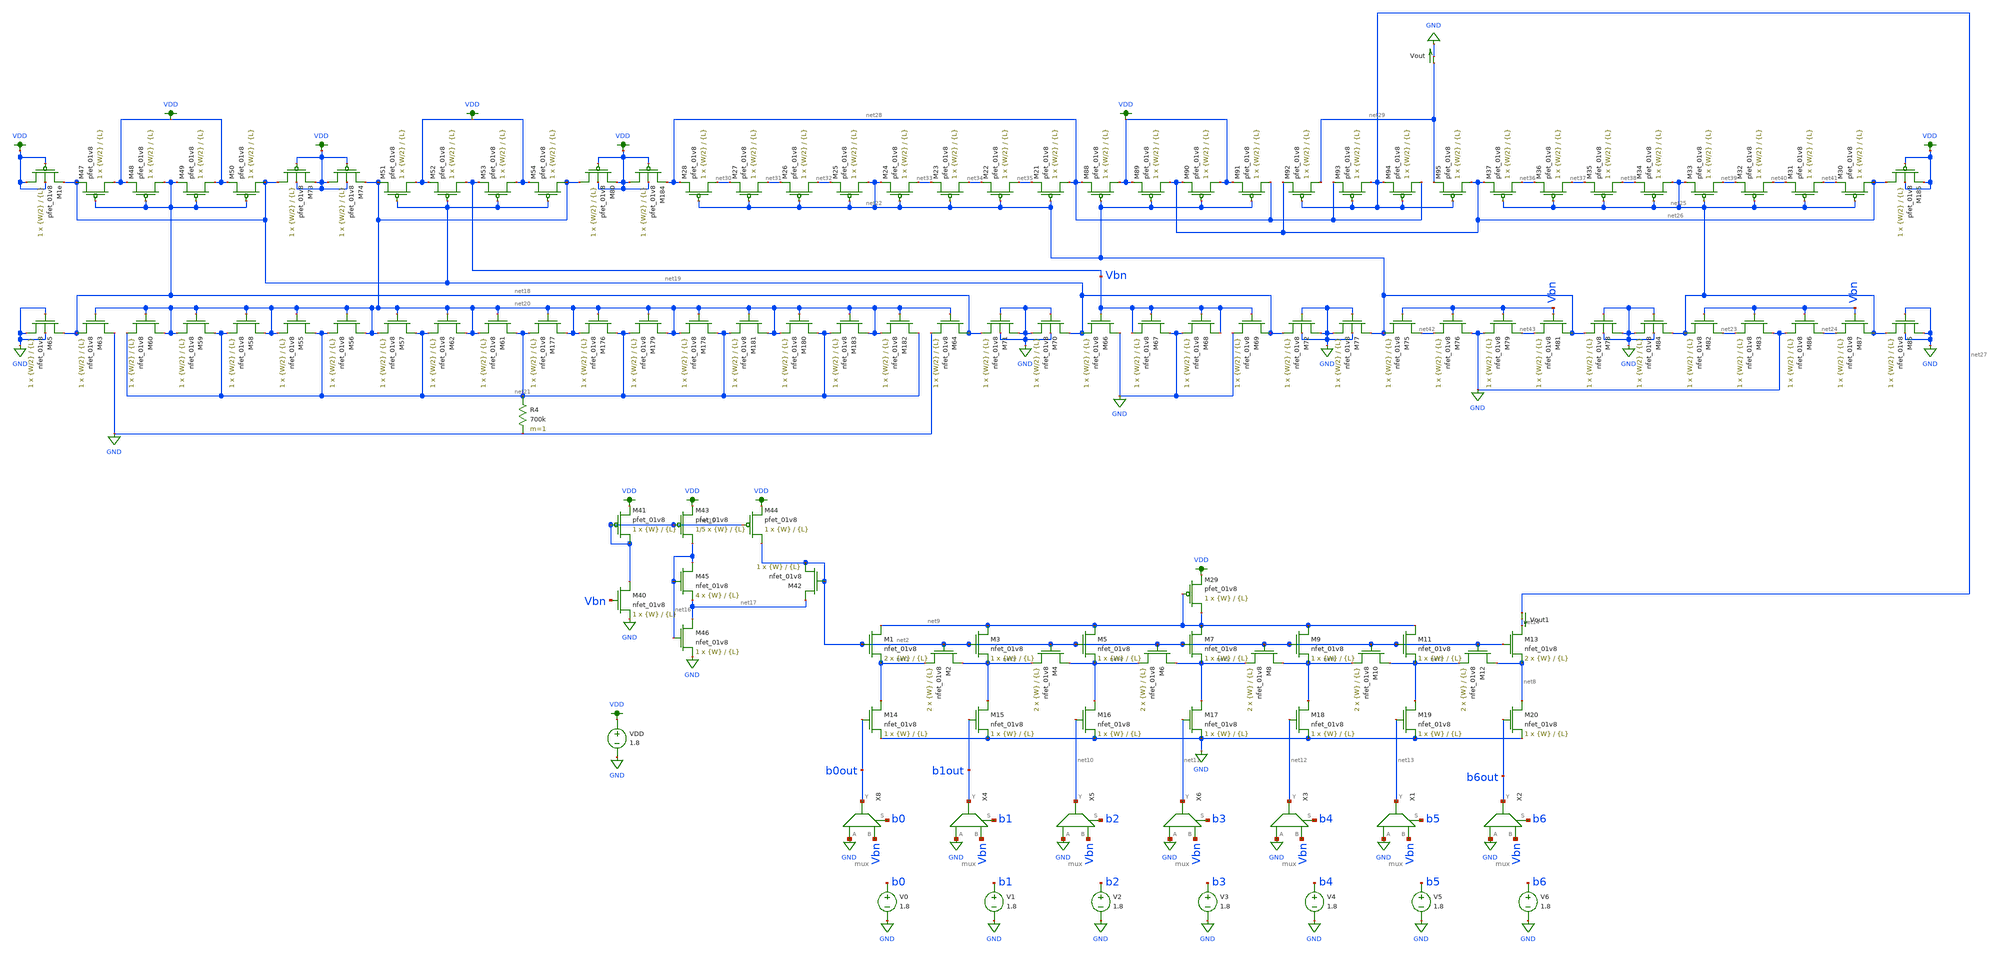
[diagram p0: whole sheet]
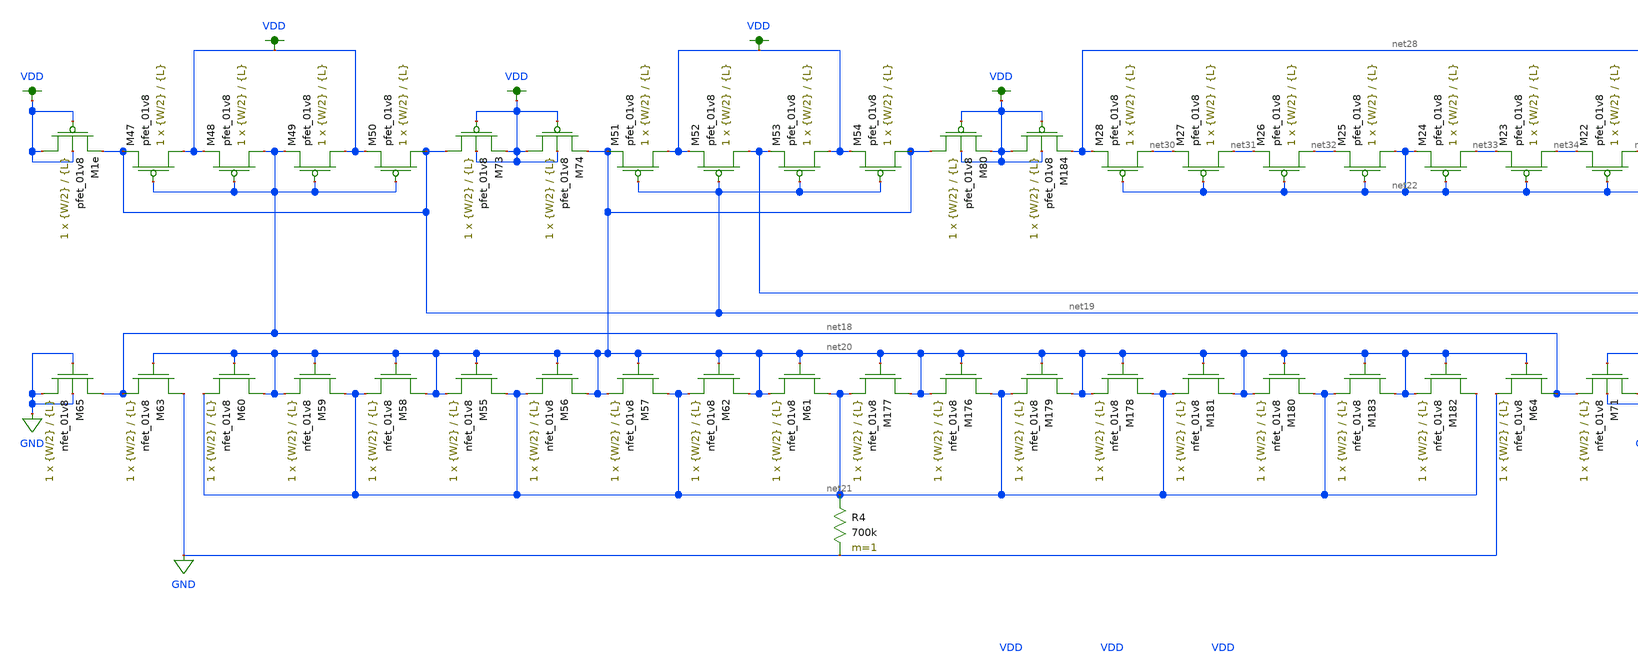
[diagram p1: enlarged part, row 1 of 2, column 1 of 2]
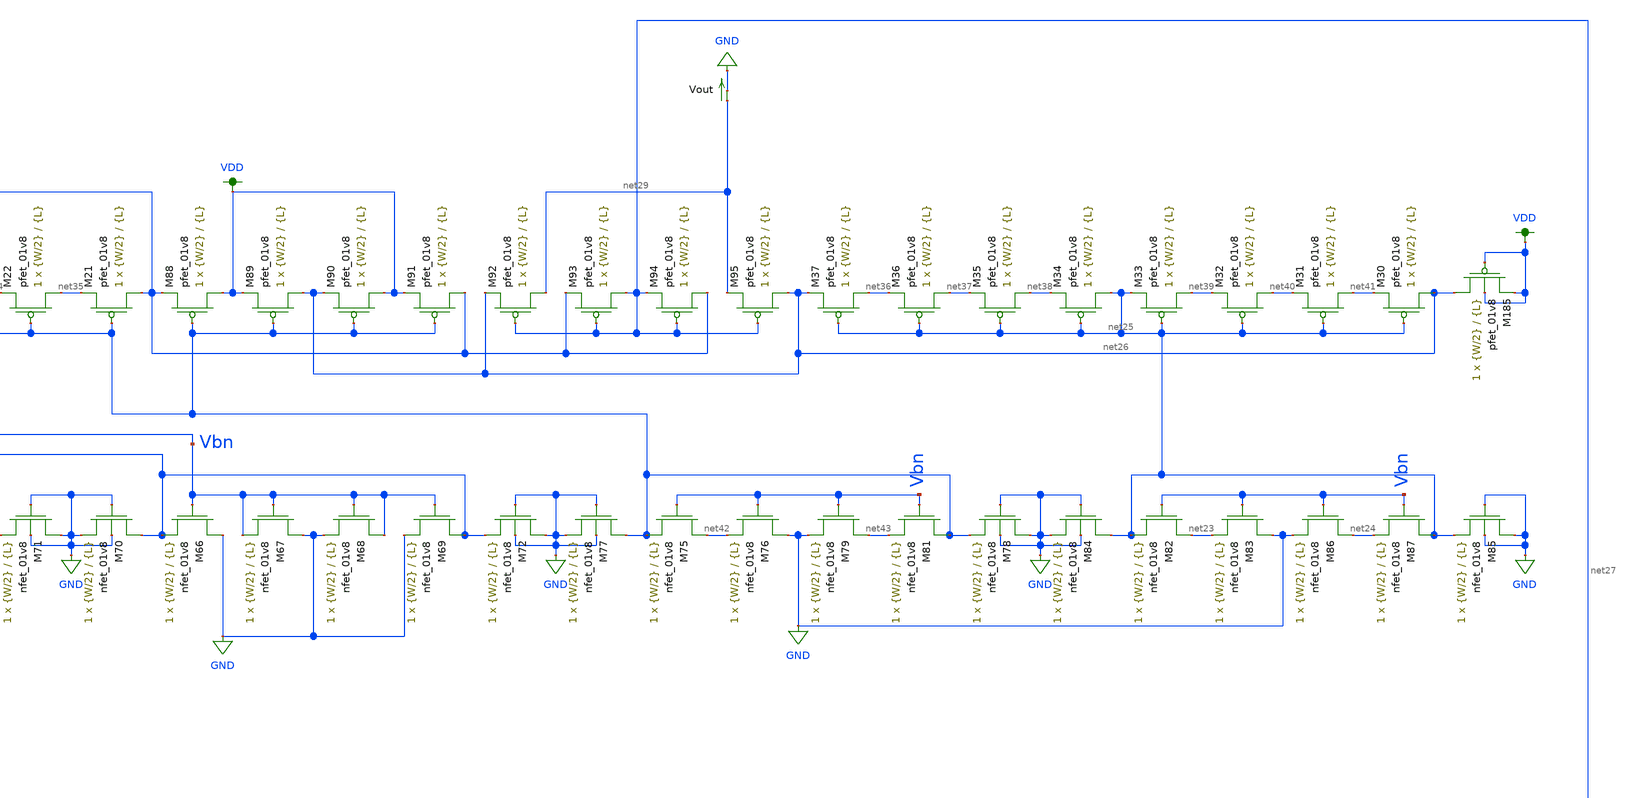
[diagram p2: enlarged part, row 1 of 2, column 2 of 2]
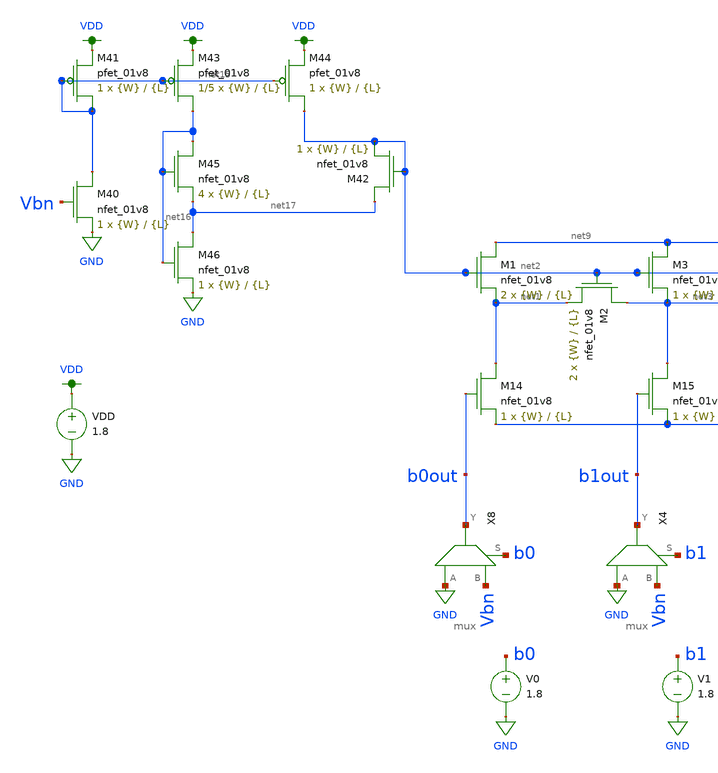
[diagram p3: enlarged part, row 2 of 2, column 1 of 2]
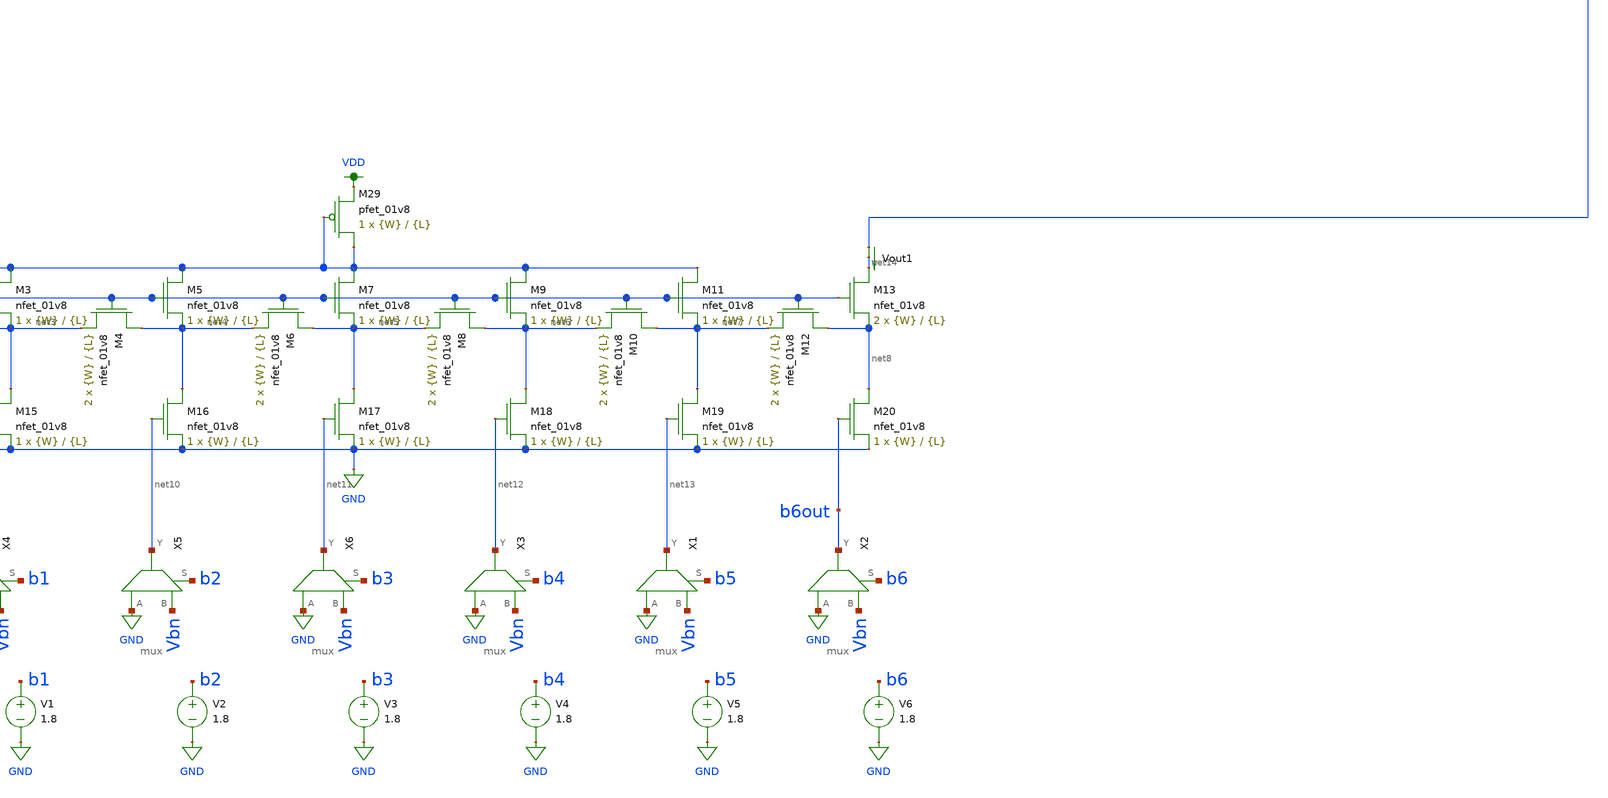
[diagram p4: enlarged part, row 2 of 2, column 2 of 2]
** sch_path: schematics/dac_dnl_inl_current_mirror_lds.sch
**.subckt dac_dnl_inl_current_mirror_lds
XM1 net9 net2 net1 GND sky130_fd_pr__nfet_01v8 L={L} W={W} nf=1 ad='int((nf+1)/2) * W/nf * 0.29' as='int((nf+2)/2) * W/nf * 0.29'
+ pd='2*int((nf+1)/2) * (W/nf + 0.29)' ps='2*int((nf+2)/2) * (W/nf + 0.29)' nrd='0.29 / W' nrs='0.29 / W'
+ sa=0 sb=0 sd=0 mult=2 m=2
XM2 net3 net2 net1 GND sky130_fd_pr__nfet_01v8 L={L} W={W} nf=1 ad='int((nf+1)/2) * W/nf * 0.29' as='int((nf+2)/2) * W/nf * 0.29'
+ pd='2*int((nf+1)/2) * (W/nf + 0.29)' ps='2*int((nf+2)/2) * (W/nf + 0.29)' nrd='0.29 / W' nrs='0.29 / W'
+ sa=0 sb=0 sd=0 mult=2 m=2
XM3 net9 net2 net3 GND sky130_fd_pr__nfet_01v8 L={L} W={W} nf=1 ad='int((nf+1)/2) * W/nf * 0.29' as='int((nf+2)/2) * W/nf * 0.29'
+ pd='2*int((nf+1)/2) * (W/nf + 0.29)' ps='2*int((nf+2)/2) * (W/nf + 0.29)' nrd='0.29 / W' nrs='0.29 / W'
+ sa=0 sb=0 sd=0 mult=1 m=1
XM4 net4 net2 net3 GND sky130_fd_pr__nfet_01v8 L={L} W={W} nf=1 ad='int((nf+1)/2) * W/nf * 0.29' as='int((nf+2)/2) * W/nf * 0.29'
+ pd='2*int((nf+1)/2) * (W/nf + 0.29)' ps='2*int((nf+2)/2) * (W/nf + 0.29)' nrd='0.29 / W' nrs='0.29 / W'
+ sa=0 sb=0 sd=0 mult=2 m=2
XM5 net9 net2 net4 GND sky130_fd_pr__nfet_01v8 L={L} W={W} nf=1 ad='int((nf+1)/2) * W/nf * 0.29' as='int((nf+2)/2) * W/nf * 0.29'
+ pd='2*int((nf+1)/2) * (W/nf + 0.29)' ps='2*int((nf+2)/2) * (W/nf + 0.29)' nrd='0.29 / W' nrs='0.29 / W'
+ sa=0 sb=0 sd=0 mult=1 m=1
XM6 net5 net2 net4 GND sky130_fd_pr__nfet_01v8 L={L} W={W} nf=1 ad='int((nf+1)/2) * W/nf * 0.29' as='int((nf+2)/2) * W/nf * 0.29'
+ pd='2*int((nf+1)/2) * (W/nf + 0.29)' ps='2*int((nf+2)/2) * (W/nf + 0.29)' nrd='0.29 / W' nrs='0.29 / W'
+ sa=0 sb=0 sd=0 mult=2 m=2
XM7 net9 net2 net5 GND sky130_fd_pr__nfet_01v8 L={L} W={W} nf=1 ad='int((nf+1)/2) * W/nf * 0.29' as='int((nf+2)/2) * W/nf * 0.29'
+ pd='2*int((nf+1)/2) * (W/nf + 0.29)' ps='2*int((nf+2)/2) * (W/nf + 0.29)' nrd='0.29 / W' nrs='0.29 / W'
+ sa=0 sb=0 sd=0 mult=1 m=1
XM8 net6 net2 net5 GND sky130_fd_pr__nfet_01v8 L={L} W={W} nf=1 ad='int((nf+1)/2) * W/nf * 0.29' as='int((nf+2)/2) * W/nf * 0.29'
+ pd='2*int((nf+1)/2) * (W/nf + 0.29)' ps='2*int((nf+2)/2) * (W/nf + 0.29)' nrd='0.29 / W' nrs='0.29 / W'
+ sa=0 sb=0 sd=0 mult=2 m=2
XM9 net9 net2 net6 GND sky130_fd_pr__nfet_01v8 L={L} W={W} nf=1 ad='int((nf+1)/2) * W/nf * 0.29' as='int((nf+2)/2) * W/nf * 0.29'
+ pd='2*int((nf+1)/2) * (W/nf + 0.29)' ps='2*int((nf+2)/2) * (W/nf + 0.29)' nrd='0.29 / W' nrs='0.29 / W'
+ sa=0 sb=0 sd=0 mult=1 m=1
XM10 net7 net2 net6 GND sky130_fd_pr__nfet_01v8 L={L} W={W} nf=1 ad='int((nf+1)/2) * W/nf * 0.29' as='int((nf+2)/2) * W/nf * 0.29'
+ pd='2*int((nf+1)/2) * (W/nf + 0.29)' ps='2*int((nf+2)/2) * (W/nf + 0.29)' nrd='0.29 / W' nrs='0.29 / W'
+ sa=0 sb=0 sd=0 mult=2 m=2
XM11 net9 net2 net7 GND sky130_fd_pr__nfet_01v8 L={L} W={W} nf=1 ad='int((nf+1)/2) * W/nf * 0.29' as='int((nf+2)/2) * W/nf * 0.29'
+ pd='2*int((nf+1)/2) * (W/nf + 0.29)' ps='2*int((nf+2)/2) * (W/nf + 0.29)' nrd='0.29 / W' nrs='0.29 / W'
+ sa=0 sb=0 sd=0 mult=1 m=1
XM12 net8 net2 net7 GND sky130_fd_pr__nfet_01v8 L={L} W={W} nf=1 ad='int((nf+1)/2) * W/nf * 0.29' as='int((nf+2)/2) * W/nf * 0.29'
+ pd='2*int((nf+1)/2) * (W/nf + 0.29)' ps='2*int((nf+2)/2) * (W/nf + 0.29)' nrd='0.29 / W' nrs='0.29 / W'
+ sa=0 sb=0 sd=0 mult=2 m=2
XM13 net14 net2 net8 GND sky130_fd_pr__nfet_01v8 L={L} W={W} nf=1 ad='int((nf+1)/2) * W/nf * 0.29' as='int((nf+2)/2) * W/nf * 0.29'
+ pd='2*int((nf+1)/2) * (W/nf + 0.29)' ps='2*int((nf+2)/2) * (W/nf + 0.29)' nrd='0.29 / W' nrs='0.29 / W'
+ sa=0 sb=0 sd=0 mult=2 m=2
XM14 net1 b0out GND GND sky130_fd_pr__nfet_01v8 L={L} W={W} nf=1 ad='int((nf+1)/2) * W/nf * 0.29' as='int((nf+2)/2) * W/nf * 0.29'
+ pd='2*int((nf+1)/2) * (W/nf + 0.29)' ps='2*int((nf+2)/2) * (W/nf + 0.29)' nrd='0.29 / W' nrs='0.29 / W'
+ sa=0 sb=0 sd=0 mult=1 m=1
XM15 net3 b1out GND GND sky130_fd_pr__nfet_01v8 L={L} W={W} nf=1 ad='int((nf+1)/2) * W/nf * 0.29' as='int((nf+2)/2) * W/nf * 0.29'
+ pd='2*int((nf+1)/2) * (W/nf + 0.29)' ps='2*int((nf+2)/2) * (W/nf + 0.29)' nrd='0.29 / W' nrs='0.29 / W'
+ sa=0 sb=0 sd=0 mult=1 m=1
XM16 net4 net10 GND GND sky130_fd_pr__nfet_01v8 L={L} W={W} nf=1 ad='int((nf+1)/2) * W/nf * 0.29' as='int((nf+2)/2) * W/nf * 0.29'
+ pd='2*int((nf+1)/2) * (W/nf + 0.29)' ps='2*int((nf+2)/2) * (W/nf + 0.29)' nrd='0.29 / W' nrs='0.29 / W'
+ sa=0 sb=0 sd=0 mult=1 m=1
XM17 net5 net11 GND GND sky130_fd_pr__nfet_01v8 L={L} W={W} nf=1 ad='int((nf+1)/2) * W/nf * 0.29' as='int((nf+2)/2) * W/nf * 0.29'
+ pd='2*int((nf+1)/2) * (W/nf + 0.29)' ps='2*int((nf+2)/2) * (W/nf + 0.29)' nrd='0.29 / W' nrs='0.29 / W'
+ sa=0 sb=0 sd=0 mult=1 m=1
XM18 net6 net12 GND GND sky130_fd_pr__nfet_01v8 L={L} W={W} nf=1 ad='int((nf+1)/2) * W/nf * 0.29' as='int((nf+2)/2) * W/nf * 0.29'
+ pd='2*int((nf+1)/2) * (W/nf + 0.29)' ps='2*int((nf+2)/2) * (W/nf + 0.29)' nrd='0.29 / W' nrs='0.29 / W'
+ sa=0 sb=0 sd=0 mult=1 m=1
XM19 net7 net13 GND GND sky130_fd_pr__nfet_01v8 L={L} W={W} nf=1 ad='int((nf+1)/2) * W/nf * 0.29' as='int((nf+2)/2) * W/nf * 0.29'
+ pd='2*int((nf+1)/2) * (W/nf + 0.29)' ps='2*int((nf+2)/2) * (W/nf + 0.29)' nrd='0.29 / W' nrs='0.29 / W'
+ sa=0 sb=0 sd=0 mult=1 m=1
XM20 net8 b6out GND GND sky130_fd_pr__nfet_01v8 L={L} W={W} nf=1 ad='int((nf+1)/2) * W/nf * 0.29' as='int((nf+2)/2) * W/nf * 0.29'
+ pd='2*int((nf+1)/2) * (W/nf + 0.29)' ps='2*int((nf+2)/2) * (W/nf + 0.29)' nrd='0.29 / W' nrs='0.29 / W'
+ sa=0 sb=0 sd=0 mult=1 m=1
V0 b0 GND 1.8
V1 b1 GND 1.8
V2 b2 GND 1.8
V3 b3 GND 1.8
V4 b4 GND 1.8
V5 b5 GND 1.8
V6 b6 GND 1.8
VDD VDD GND 1.8
XM29 net9 net9 VDD VDD sky130_fd_pr__pfet_01v8 L={L} W={W} nf=1 ad='int((nf+1)/2) * W/nf * 0.29' as='int((nf+2)/2) * W/nf * 0.29'
+ pd='2*int((nf+1)/2) * (W/nf + 0.29)' ps='2*int((nf+2)/2) * (W/nf + 0.29)' nrd='0.29 / W' nrs='0.29 / W'
+ sa=0 sb=0 sd=0 mult=1 m=1
X8 GND Vbn b0out b0 mux
X4 GND Vbn b1out b1 mux
X5 GND Vbn net10 b2 mux
X6 GND Vbn net11 b3 mux
X3 GND Vbn net12 b4 mux
X1 GND Vbn net13 b5 mux
X2 GND Vbn b6out b6 mux
Vout1 net27 net14 0
.save i(vout1)
XM40 net15 Vbn GND GND sky130_fd_pr__nfet_01v8 L={L} W={W} nf=1 ad='int((nf+1)/2) * W/nf * 0.29' as='int((nf+2)/2) * W/nf * 0.29'
+ pd='2*int((nf+1)/2) * (W/nf + 0.29)' ps='2*int((nf+2)/2) * (W/nf + 0.29)' nrd='0.29 / W' nrs='0.29 / W'
+ sa=0 sb=0 sd=0 mult=1 m=1
XM41 net15 net15 VDD VDD sky130_fd_pr__pfet_01v8 L={L} W={W} nf=1 ad='int((nf+1)/2) * W/nf * 0.29' as='int((nf+2)/2) * W/nf * 0.29'
+ pd='2*int((nf+1)/2) * (W/nf + 0.29)' ps='2*int((nf+2)/2) * (W/nf + 0.29)' nrd='0.29 / W' nrs='0.29 / W'
+ sa=0 sb=0 sd=0 mult=1 m=1
XM42 net17 net2 net2 GND sky130_fd_pr__nfet_01v8 L={L} W={W} nf=1 ad='int((nf+1)/2) * W/nf * 0.29' as='int((nf+2)/2) * W/nf * 0.29'
+ pd='2*int((nf+1)/2) * (W/nf + 0.29)' ps='2*int((nf+2)/2) * (W/nf + 0.29)' nrd='0.29 / W' nrs='0.29 / W'
+ sa=0 sb=0 sd=0 mult=1 m=1
XM43 net16 net15 VDD VDD sky130_fd_pr__pfet_01v8 L={L} W={W} nf=1 ad='int((nf+1)/2) * W/nf * 0.29' as='int((nf+2)/2) * W/nf * 0.29'
+ pd='2*int((nf+1)/2) * (W/nf + 0.29)' ps='2*int((nf+2)/2) * (W/nf + 0.29)' nrd='0.29 / W' nrs='0.29 / W'
+ sa=0 sb=0 sd=0 mult=1/5 m=1/5
XM44 net2 net15 VDD VDD sky130_fd_pr__pfet_01v8 L={L} W={W} nf=1 ad='int((nf+1)/2) * W/nf * 0.29' as='int((nf+2)/2) * W/nf * 0.29'
+ pd='2*int((nf+1)/2) * (W/nf + 0.29)' ps='2*int((nf+2)/2) * (W/nf + 0.29)' nrd='0.29 / W' nrs='0.29 / W'
+ sa=0 sb=0 sd=0 mult=1 m=1
XM45 net16 net16 net17 GND sky130_fd_pr__nfet_01v8 L={L} W={W} nf=1 ad='int((nf+1)/2) * W/nf * 0.29'
+ as='int((nf+2)/2) * W/nf * 0.29' pd='2*int((nf+1)/2) * (W/nf + 0.29)' ps='2*int((nf+2)/2) * (W/nf + 0.29)'
+ nrd='0.29 / W' nrs='0.29 / W' sa=0 sb=0 sd=0 mult=4 m=4
XM46 net17 net16 GND GND sky130_fd_pr__nfet_01v8 L={L} W={W} nf=1 ad='int((nf+1)/2) * W/nf * 0.29' as='int((nf+2)/2) * W/nf * 0.29'
+ pd='2*int((nf+1)/2) * (W/nf + 0.29)' ps='2*int((nf+2)/2) * (W/nf + 0.29)' nrd='0.29 / W' nrs='0.29 / W'
+ sa=0 sb=0 sd=0 mult=1 m=1
XM47 VDD net18 net19 VDD sky130_fd_pr__pfet_01v8 L={L} W={W/2} nf=1 ad='int((nf+1)/2) * W/nf * 0.29'
+ as='int((nf+2)/2) * W/nf * 0.29' pd='2*int((nf+1)/2) * (W/nf + 0.29)' ps='2*int((nf+2)/2) * (W/nf + 0.29)'
+ nrd='0.29 / W' nrs='0.29 / W' sa=0 sb=0 sd=0 mult=1 m=1
XM48 net18 net18 VDD VDD sky130_fd_pr__pfet_01v8 L={L} W={W/2} nf=1 ad='int((nf+1)/2) * W/nf * 0.29'
+ as='int((nf+2)/2) * W/nf * 0.29' pd='2*int((nf+1)/2) * (W/nf + 0.29)' ps='2*int((nf+2)/2) * (W/nf + 0.29)'
+ nrd='0.29 / W' nrs='0.29 / W' sa=0 sb=0 sd=0 mult=1 m=1
XM49 VDD net18 net18 VDD sky130_fd_pr__pfet_01v8 L={L} W={W/2} nf=1 ad='int((nf+1)/2) * W/nf * 0.29'
+ as='int((nf+2)/2) * W/nf * 0.29' pd='2*int((nf+1)/2) * (W/nf + 0.29)' ps='2*int((nf+2)/2) * (W/nf + 0.29)'
+ nrd='0.29 / W' nrs='0.29 / W' sa=0 sb=0 sd=0 mult=1 m=1
XM50 net19 net18 VDD VDD sky130_fd_pr__pfet_01v8 L={L} W={W/2} nf=1 ad='int((nf+1)/2) * W/nf * 0.29'
+ as='int((nf+2)/2) * W/nf * 0.29' pd='2*int((nf+1)/2) * (W/nf + 0.29)' ps='2*int((nf+2)/2) * (W/nf + 0.29)'
+ nrd='0.29 / W' nrs='0.29 / W' sa=0 sb=0 sd=0 mult=1 m=1
XM51 VDD net19 net20 VDD sky130_fd_pr__pfet_01v8 L={L} W={W/2} nf=1 ad='int((nf+1)/2) * W/nf * 0.29'
+ as='int((nf+2)/2) * W/nf * 0.29' pd='2*int((nf+1)/2) * (W/nf + 0.29)' ps='2*int((nf+2)/2) * (W/nf + 0.29)'
+ nrd='0.29 / W' nrs='0.29 / W' sa=0 sb=0 sd=0 mult=1 m=1
XM52 Vbn net19 VDD VDD sky130_fd_pr__pfet_01v8 L={L} W={W/2} nf=1 ad='int((nf+1)/2) * W/nf * 0.29' as='int((nf+2)/2) * W/nf * 0.29'
+ pd='2*int((nf+1)/2) * (W/nf + 0.29)' ps='2*int((nf+2)/2) * (W/nf + 0.29)' nrd='0.29 / W' nrs='0.29 / W'
+ sa=0 sb=0 sd=0 mult=1 m=1
XM53 VDD net19 Vbn VDD sky130_fd_pr__pfet_01v8 L={L} W={W/2} nf=1 ad='int((nf+1)/2) * W/nf * 0.29' as='int((nf+2)/2) * W/nf * 0.29'
+ pd='2*int((nf+1)/2) * (W/nf + 0.29)' ps='2*int((nf+2)/2) * (W/nf + 0.29)' nrd='0.29 / W' nrs='0.29 / W'
+ sa=0 sb=0 sd=0 mult=1 m=1
XM54 net20 net19 VDD VDD sky130_fd_pr__pfet_01v8 L={L} W={W/2} nf=1 ad='int((nf+1)/2) * W/nf * 0.29'
+ as='int((nf+2)/2) * W/nf * 0.29' pd='2*int((nf+1)/2) * (W/nf + 0.29)' ps='2*int((nf+2)/2) * (W/nf + 0.29)'
+ nrd='0.29 / W' nrs='0.29 / W' sa=0 sb=0 sd=0 mult=1 m=1
XM55 net21 net20 net20 GND sky130_fd_pr__nfet_01v8 L={L} W={W/2} nf=1 ad='int((nf+1)/2) * W/nf * 0.29'
+ as='int((nf+2)/2) * W/nf * 0.29' pd='2*int((nf+1)/2) * (W/nf + 0.29)' ps='2*int((nf+2)/2) * (W/nf + 0.29)'
+ nrd='0.29 / W' nrs='0.29 / W' sa=0 sb=0 sd=0 mult=1 m=1
XM56 net20 net20 net21 GND sky130_fd_pr__nfet_01v8 L={L} W={W/2} nf=1 ad='int((nf+1)/2) * W/nf * 0.29'
+ as='int((nf+2)/2) * W/nf * 0.29' pd='2*int((nf+1)/2) * (W/nf + 0.29)' ps='2*int((nf+2)/2) * (W/nf + 0.29)'
+ nrd='0.29 / W' nrs='0.29 / W' sa=0 sb=0 sd=0 mult=1 m=1
XM57 net21 net20 net20 GND sky130_fd_pr__nfet_01v8 L={L} W={W/2} nf=1 ad='int((nf+1)/2) * W/nf * 0.29'
+ as='int((nf+2)/2) * W/nf * 0.29' pd='2*int((nf+1)/2) * (W/nf + 0.29)' ps='2*int((nf+2)/2) * (W/nf + 0.29)'
+ nrd='0.29 / W' nrs='0.29 / W' sa=0 sb=0 sd=0 mult=1 m=1
XM58 net20 net20 net21 GND sky130_fd_pr__nfet_01v8 L={L} W={W/2} nf=1 ad='int((nf+1)/2) * W/nf * 0.29'
+ as='int((nf+2)/2) * W/nf * 0.29' pd='2*int((nf+1)/2) * (W/nf + 0.29)' ps='2*int((nf+2)/2) * (W/nf + 0.29)'
+ nrd='0.29 / W' nrs='0.29 / W' sa=0 sb=0 sd=0 mult=1 m=1
XM59 net21 net20 net20 GND sky130_fd_pr__nfet_01v8 L={L} W={W/2} nf=1 ad='int((nf+1)/2) * W/nf * 0.29'
+ as='int((nf+2)/2) * W/nf * 0.29' pd='2*int((nf+1)/2) * (W/nf + 0.29)' ps='2*int((nf+2)/2) * (W/nf + 0.29)'
+ nrd='0.29 / W' nrs='0.29 / W' sa=0 sb=0 sd=0 mult=1 m=1
XM60 net20 net20 net21 GND sky130_fd_pr__nfet_01v8 L={L} W={W/2} nf=1 ad='int((nf+1)/2) * W/nf * 0.29'
+ as='int((nf+2)/2) * W/nf * 0.29' pd='2*int((nf+1)/2) * (W/nf + 0.29)' ps='2*int((nf+2)/2) * (W/nf + 0.29)'
+ nrd='0.29 / W' nrs='0.29 / W' sa=0 sb=0 sd=0 mult=1 m=1
XM61 net21 net20 net20 GND sky130_fd_pr__nfet_01v8 L={L} W={W/2} nf=1 ad='int((nf+1)/2) * W/nf * 0.29'
+ as='int((nf+2)/2) * W/nf * 0.29' pd='2*int((nf+1)/2) * (W/nf + 0.29)' ps='2*int((nf+2)/2) * (W/nf + 0.29)'
+ nrd='0.29 / W' nrs='0.29 / W' sa=0 sb=0 sd=0 mult=1 m=1
XM62 net20 net20 net21 GND sky130_fd_pr__nfet_01v8 L={L} W={W/2} nf=1 ad='int((nf+1)/2) * W/nf * 0.29'
+ as='int((nf+2)/2) * W/nf * 0.29' pd='2*int((nf+1)/2) * (W/nf + 0.29)' ps='2*int((nf+2)/2) * (W/nf + 0.29)'
+ nrd='0.29 / W' nrs='0.29 / W' sa=0 sb=0 sd=0 mult=1 m=1
XM63 GND net20 net18 GND sky130_fd_pr__nfet_01v8 L={L} W={W/2} nf=1 ad='int((nf+1)/2) * W/nf * 0.29'
+ as='int((nf+2)/2) * W/nf * 0.29' pd='2*int((nf+1)/2) * (W/nf + 0.29)' ps='2*int((nf+2)/2) * (W/nf + 0.29)'
+ nrd='0.29 / W' nrs='0.29 / W' sa=0 sb=0 sd=0 mult=1 m=1
XM64 net18 net20 GND GND sky130_fd_pr__nfet_01v8 L={L} W={W/2} nf=1 ad='int((nf+1)/2) * W/nf * 0.29'
+ as='int((nf+2)/2) * W/nf * 0.29' pd='2*int((nf+1)/2) * (W/nf + 0.29)' ps='2*int((nf+2)/2) * (W/nf + 0.29)'
+ nrd='0.29 / W' nrs='0.29 / W' sa=0 sb=0 sd=0 mult=1 m=1
R4 net21 GND 700k m=1
XM1e VDD VDD net19 VDD sky130_fd_pr__pfet_01v8 L={L} W={W/2} nf=1 ad='int((nf+1)/2) * W/nf * 0.29' as='int((nf+2)/2) * W/nf * 0.29'
+ pd='2*int((nf+1)/2) * (W/nf + 0.29)' ps='2*int((nf+2)/2) * (W/nf + 0.29)' nrd='0.29 / W' nrs='0.29 / W'
+ sa=0 sb=0 sd=0 mult=1 m=1
XM65 net18 GND GND GND sky130_fd_pr__nfet_01v8 L={L} W={W/2} nf=1 ad='int((nf+1)/2) * W/nf * 0.29' as='int((nf+2)/2) * W/nf * 0.29'
+ pd='2*int((nf+1)/2) * (W/nf + 0.29)' ps='2*int((nf+2)/2) * (W/nf + 0.29)' nrd='0.29 / W' nrs='0.29 / W'
+ sa=0 sb=0 sd=0 mult=1 m=1
XM66 GND Vbn net19 GND sky130_fd_pr__nfet_01v8 L={L} W={W/2} nf=1 ad='int((nf+1)/2) * W/nf * 0.29' as='int((nf+2)/2) * W/nf * 0.29'
+ pd='2*int((nf+1)/2) * (W/nf + 0.29)' ps='2*int((nf+2)/2) * (W/nf + 0.29)' nrd='0.29 / W' nrs='0.29 / W'
+ sa=0 sb=0 sd=0 mult=1 m=1
XM67 GND Vbn Vbn GND sky130_fd_pr__nfet_01v8 L={L} W={W/2} nf=1 ad='int((nf+1)/2) * W/nf * 0.29' as='int((nf+2)/2) * W/nf * 0.29'
+ pd='2*int((nf+1)/2) * (W/nf + 0.29)' ps='2*int((nf+2)/2) * (W/nf + 0.29)' nrd='0.29 / W' nrs='0.29 / W'
+ sa=0 sb=0 sd=0 mult=1 m=1
XM68 Vbn Vbn GND GND sky130_fd_pr__nfet_01v8 L={L} W={W/2} nf=1 ad='int((nf+1)/2) * W/nf * 0.29' as='int((nf+2)/2) * W/nf * 0.29'
+ pd='2*int((nf+1)/2) * (W/nf + 0.29)' ps='2*int((nf+2)/2) * (W/nf + 0.29)' nrd='0.29 / W' nrs='0.29 / W'
+ sa=0 sb=0 sd=0 mult=1 m=1
XM69 net19 Vbn GND GND sky130_fd_pr__nfet_01v8 L={L} W={W/2} nf=1 ad='int((nf+1)/2) * W/nf * 0.29' as='int((nf+2)/2) * W/nf * 0.29'
+ pd='2*int((nf+1)/2) * (W/nf + 0.29)' ps='2*int((nf+2)/2) * (W/nf + 0.29)' nrd='0.29 / W' nrs='0.29 / W'
+ sa=0 sb=0 sd=0 mult=1 m=1
XM70 net19 GND GND GND sky130_fd_pr__nfet_01v8 L={L} W={W/2} nf=1 ad='int((nf+1)/2) * W/nf * 0.29' as='int((nf+2)/2) * W/nf * 0.29'
+ pd='2*int((nf+1)/2) * (W/nf + 0.29)' ps='2*int((nf+2)/2) * (W/nf + 0.29)' nrd='0.29 / W' nrs='0.29 / W'
+ sa=0 sb=0 sd=0 mult=1 m=1
XM71 GND GND net18 GND sky130_fd_pr__nfet_01v8 L={L} W={W/2} nf=1 ad='int((nf+1)/2) * W/nf * 0.29' as='int((nf+2)/2) * W/nf * 0.29'
+ pd='2*int((nf+1)/2) * (W/nf + 0.29)' ps='2*int((nf+2)/2) * (W/nf + 0.29)' nrd='0.29 / W' nrs='0.29 / W'
+ sa=0 sb=0 sd=0 mult=1 m=1
XM72 GND GND net19 GND sky130_fd_pr__nfet_01v8 L={L} W={W/2} nf=1 ad='int((nf+1)/2) * W/nf * 0.29' as='int((nf+2)/2) * W/nf * 0.29'
+ pd='2*int((nf+1)/2) * (W/nf + 0.29)' ps='2*int((nf+2)/2) * (W/nf + 0.29)' nrd='0.29 / W' nrs='0.29 / W'
+ sa=0 sb=0 sd=0 mult=1 m=1
XM77 net22 GND GND GND sky130_fd_pr__nfet_01v8 L={L} W={W/2} nf=1 ad='int((nf+1)/2) * W/nf * 0.29' as='int((nf+2)/2) * W/nf * 0.29'
+ pd='2*int((nf+1)/2) * (W/nf + 0.29)' ps='2*int((nf+2)/2) * (W/nf + 0.29)' nrd='0.29 / W' nrs='0.29 / W'
+ sa=0 sb=0 sd=0 mult=1 m=1
XM78 GND GND net22 GND sky130_fd_pr__nfet_01v8 L={L} W={W/2} nf=1 ad='int((nf+1)/2) * W/nf * 0.29' as='int((nf+2)/2) * W/nf * 0.29'
+ pd='2*int((nf+1)/2) * (W/nf + 0.29)' ps='2*int((nf+2)/2) * (W/nf + 0.29)' nrd='0.29 / W' nrs='0.29 / W'
+ sa=0 sb=0 sd=0 mult=1 m=1
XM73 net19 VDD VDD VDD sky130_fd_pr__pfet_01v8 L={L} W={W/2} nf=1 ad='int((nf+1)/2) * W/nf * 0.29' as='int((nf+2)/2) * W/nf * 0.29'
+ pd='2*int((nf+1)/2) * (W/nf + 0.29)' ps='2*int((nf+2)/2) * (W/nf + 0.29)' nrd='0.29 / W' nrs='0.29 / W'
+ sa=0 sb=0 sd=0 mult=1 m=1
XM74 VDD VDD net20 VDD sky130_fd_pr__pfet_01v8 L={L} W={W/2} nf=1 ad='int((nf+1)/2) * W/nf * 0.29' as='int((nf+2)/2) * W/nf * 0.29'
+ pd='2*int((nf+1)/2) * (W/nf + 0.29)' ps='2*int((nf+2)/2) * (W/nf + 0.29)' nrd='0.29 / W' nrs='0.29 / W'
+ sa=0 sb=0 sd=0 mult=1 m=1
XM80 net20 VDD VDD VDD sky130_fd_pr__pfet_01v8 L={L} W={W/2} nf=1 ad='int((nf+1)/2) * W/nf * 0.29' as='int((nf+2)/2) * W/nf * 0.29'
+ pd='2*int((nf+1)/2) * (W/nf + 0.29)' ps='2*int((nf+2)/2) * (W/nf + 0.29)' nrd='0.29 / W' nrs='0.29 / W'
+ sa=0 sb=0 sd=0 mult=1 m=1
XM84 net25 GND GND GND sky130_fd_pr__nfet_01v8 L={L} W={W/2} nf=1 ad='int((nf+1)/2) * W/nf * 0.29' as='int((nf+2)/2) * W/nf * 0.29'
+ pd='2*int((nf+1)/2) * (W/nf + 0.29)' ps='2*int((nf+2)/2) * (W/nf + 0.29)' nrd='0.29 / W' nrs='0.29 / W'
+ sa=0 sb=0 sd=0 mult=1 m=1
XM85 GND GND net25 GND sky130_fd_pr__nfet_01v8 L={L} W={W/2} nf=1 ad='int((nf+1)/2) * W/nf * 0.29' as='int((nf+2)/2) * W/nf * 0.29'
+ pd='2*int((nf+1)/2) * (W/nf + 0.29)' ps='2*int((nf+2)/2) * (W/nf + 0.29)' nrd='0.29 / W' nrs='0.29 / W'
+ sa=0 sb=0 sd=0 mult=1 m=1
XM75 net42 Vbn net22 GND sky130_fd_pr__nfet_01v8 L={L} W={W/2} nf=1 ad='int((nf+1)/2) * W/nf * 0.29'
+ as='int((nf+2)/2) * W/nf * 0.29' pd='2*int((nf+1)/2) * (W/nf + 0.29)' ps='2*int((nf+2)/2) * (W/nf + 0.29)'
+ nrd='0.29 / W' nrs='0.29 / W' sa=0 sb=0 sd=0 mult=1 m=1
XM76 GND Vbn net42 GND sky130_fd_pr__nfet_01v8 L={L} W={W/2} nf=1 ad='int((nf+1)/2) * W/nf * 0.29' as='int((nf+2)/2) * W/nf * 0.29'
+ pd='2*int((nf+1)/2) * (W/nf + 0.29)' ps='2*int((nf+2)/2) * (W/nf + 0.29)' nrd='0.29 / W' nrs='0.29 / W'
+ sa=0 sb=0 sd=0 mult=1 m=1
XM79 net43 Vbn GND GND sky130_fd_pr__nfet_01v8 L={L} W={W/2} nf=1 ad='int((nf+1)/2) * W/nf * 0.29' as='int((nf+2)/2) * W/nf * 0.29'
+ pd='2*int((nf+1)/2) * (W/nf + 0.29)' ps='2*int((nf+2)/2) * (W/nf + 0.29)' nrd='0.29 / W' nrs='0.29 / W'
+ sa=0 sb=0 sd=0 mult=1 m=1
XM81 net22 Vbn net43 GND sky130_fd_pr__nfet_01v8 L={L} W={W/2} nf=1 ad='int((nf+1)/2) * W/nf * 0.29'
+ as='int((nf+2)/2) * W/nf * 0.29' pd='2*int((nf+1)/2) * (W/nf + 0.29)' ps='2*int((nf+2)/2) * (W/nf + 0.29)'
+ nrd='0.29 / W' nrs='0.29 / W' sa=0 sb=0 sd=0 mult=1 m=1
XM82 net23 Vbn net25 GND sky130_fd_pr__nfet_01v8 L={L} W={W/2} nf=1 ad='int((nf+1)/2) * W/nf * 0.29'
+ as='int((nf+2)/2) * W/nf * 0.29' pd='2*int((nf+1)/2) * (W/nf + 0.29)' ps='2*int((nf+2)/2) * (W/nf + 0.29)'
+ nrd='0.29 / W' nrs='0.29 / W' sa=0 sb=0 sd=0 mult=1 m=1
XM83 GND Vbn net23 GND sky130_fd_pr__nfet_01v8 L={L} W={W/2} nf=1 ad='int((nf+1)/2) * W/nf * 0.29' as='int((nf+2)/2) * W/nf * 0.29'
+ pd='2*int((nf+1)/2) * (W/nf + 0.29)' ps='2*int((nf+2)/2) * (W/nf + 0.29)' nrd='0.29 / W' nrs='0.29 / W'
+ sa=0 sb=0 sd=0 mult=1 m=1
XM86 net24 Vbn GND GND sky130_fd_pr__nfet_01v8 L={L} W={W/2} nf=1 ad='int((nf+1)/2) * W/nf * 0.29' as='int((nf+2)/2) * W/nf * 0.29'
+ pd='2*int((nf+1)/2) * (W/nf + 0.29)' ps='2*int((nf+2)/2) * (W/nf + 0.29)' nrd='0.29 / W' nrs='0.29 / W'
+ sa=0 sb=0 sd=0 mult=1 m=1
XM87 net25 Vbn net24 GND sky130_fd_pr__nfet_01v8 L={L} W={W/2} nf=1 ad='int((nf+1)/2) * W/nf * 0.29'
+ as='int((nf+2)/2) * W/nf * 0.29' pd='2*int((nf+1)/2) * (W/nf + 0.29)' ps='2*int((nf+2)/2) * (W/nf + 0.29)'
+ nrd='0.29 / W' nrs='0.29 / W' sa=0 sb=0 sd=0 mult=1 m=1
XM88 VDD net22 net28 VDD sky130_fd_pr__pfet_01v8 L={L} W={W/2} nf=1 ad='int((nf+1)/2) * W/nf * 0.29'
+ as='int((nf+2)/2) * W/nf * 0.29' pd='2*int((nf+1)/2) * (W/nf + 0.29)' ps='2*int((nf+2)/2) * (W/nf + 0.29)'
+ nrd='0.29 / W' nrs='0.29 / W' sa=0 sb=0 sd=0 mult=1 m=1
XM89 net26 net22 VDD VDD sky130_fd_pr__pfet_01v8 L={L} W={W/2} nf=1 ad='int((nf+1)/2) * W/nf * 0.29'
+ as='int((nf+2)/2) * W/nf * 0.29' pd='2*int((nf+1)/2) * (W/nf + 0.29)' ps='2*int((nf+2)/2) * (W/nf + 0.29)'
+ nrd='0.29 / W' nrs='0.29 / W' sa=0 sb=0 sd=0 mult=1 m=1
XM90 VDD net22 net26 VDD sky130_fd_pr__pfet_01v8 L={L} W={W/2} nf=1 ad='int((nf+1)/2) * W/nf * 0.29'
+ as='int((nf+2)/2) * W/nf * 0.29' pd='2*int((nf+1)/2) * (W/nf + 0.29)' ps='2*int((nf+2)/2) * (W/nf + 0.29)'
+ nrd='0.29 / W' nrs='0.29 / W' sa=0 sb=0 sd=0 mult=1 m=1
XM91 net28 net22 VDD VDD sky130_fd_pr__pfet_01v8 L={L} W={W/2} nf=1 ad='int((nf+1)/2) * W/nf * 0.29'
+ as='int((nf+2)/2) * W/nf * 0.29' pd='2*int((nf+1)/2) * (W/nf + 0.29)' ps='2*int((nf+2)/2) * (W/nf + 0.29)'
+ nrd='0.29 / W' nrs='0.29 / W' sa=0 sb=0 sd=0 mult=1 m=1
XM92 net29 net27 net26 VDD sky130_fd_pr__pfet_01v8 L={L} W={W/2} nf=1 ad='int((nf+1)/2) * W/nf * 0.29'
+ as='int((nf+2)/2) * W/nf * 0.29' pd='2*int((nf+1)/2) * (W/nf + 0.29)' ps='2*int((nf+2)/2) * (W/nf + 0.29)'
+ nrd='0.29 / W' nrs='0.29 / W' sa=0 sb=0 sd=0 mult=1 m=1
XM93 net27 net27 net28 VDD sky130_fd_pr__pfet_01v8 L={L} W={W/2} nf=1 ad='int((nf+1)/2) * W/nf * 0.29'
+ as='int((nf+2)/2) * W/nf * 0.29' pd='2*int((nf+1)/2) * (W/nf + 0.29)' ps='2*int((nf+2)/2) * (W/nf + 0.29)'
+ nrd='0.29 / W' nrs='0.29 / W' sa=0 sb=0 sd=0 mult=1 m=1
XM94 net28 net27 net27 VDD sky130_fd_pr__pfet_01v8 L={L} W={W/2} nf=1 ad='int((nf+1)/2) * W/nf * 0.29'
+ as='int((nf+2)/2) * W/nf * 0.29' pd='2*int((nf+1)/2) * (W/nf + 0.29)' ps='2*int((nf+2)/2) * (W/nf + 0.29)'
+ nrd='0.29 / W' nrs='0.29 / W' sa=0 sb=0 sd=0 mult=1 m=1
XM95 net26 net27 net29 VDD sky130_fd_pr__pfet_01v8 L={L} W={W/2} nf=1 ad='int((nf+1)/2) * W/nf * 0.29'
+ as='int((nf+2)/2) * W/nf * 0.29' pd='2*int((nf+1)/2) * (W/nf + 0.29)' ps='2*int((nf+2)/2) * (W/nf + 0.29)'
+ nrd='0.29 / W' nrs='0.29 / W' sa=0 sb=0 sd=0 mult=1 m=1
XM176 net21 net20 net20 GND sky130_fd_pr__nfet_01v8 L={L} W={W/2} nf=1 ad='int((nf+1)/2) * W/nf * 0.29'
+ as='int((nf+2)/2) * W/nf * 0.29' pd='2*int((nf+1)/2) * (W/nf + 0.29)' ps='2*int((nf+2)/2) * (W/nf + 0.29)'
+ nrd='0.29 / W' nrs='0.29 / W' sa=0 sb=0 sd=0 mult=1 m=1
XM177 net20 net20 net21 GND sky130_fd_pr__nfet_01v8 L={L} W={W/2} nf=1 ad='int((nf+1)/2) * W/nf * 0.29'
+ as='int((nf+2)/2) * W/nf * 0.29' pd='2*int((nf+1)/2) * (W/nf + 0.29)' ps='2*int((nf+2)/2) * (W/nf + 0.29)'
+ nrd='0.29 / W' nrs='0.29 / W' sa=0 sb=0 sd=0 mult=1 m=1
XM178 net21 net20 net20 GND sky130_fd_pr__nfet_01v8 L={L} W={W/2} nf=1 ad='int((nf+1)/2) * W/nf * 0.29'
+ as='int((nf+2)/2) * W/nf * 0.29' pd='2*int((nf+1)/2) * (W/nf + 0.29)' ps='2*int((nf+2)/2) * (W/nf + 0.29)'
+ nrd='0.29 / W' nrs='0.29 / W' sa=0 sb=0 sd=0 mult=1 m=1
XM179 net20 net20 net21 GND sky130_fd_pr__nfet_01v8 L={L} W={W/2} nf=1 ad='int((nf+1)/2) * W/nf * 0.29'
+ as='int((nf+2)/2) * W/nf * 0.29' pd='2*int((nf+1)/2) * (W/nf + 0.29)' ps='2*int((nf+2)/2) * (W/nf + 0.29)'
+ nrd='0.29 / W' nrs='0.29 / W' sa=0 sb=0 sd=0 mult=1 m=1
XM180 net21 net20 net20 GND sky130_fd_pr__nfet_01v8 L={L} W={W/2} nf=1 ad='int((nf+1)/2) * W/nf * 0.29'
+ as='int((nf+2)/2) * W/nf * 0.29' pd='2*int((nf+1)/2) * (W/nf + 0.29)' ps='2*int((nf+2)/2) * (W/nf + 0.29)'
+ nrd='0.29 / W' nrs='0.29 / W' sa=0 sb=0 sd=0 mult=1 m=1
XM181 net20 net20 net21 GND sky130_fd_pr__nfet_01v8 L={L} W={W/2} nf=1 ad='int((nf+1)/2) * W/nf * 0.29'
+ as='int((nf+2)/2) * W/nf * 0.29' pd='2*int((nf+1)/2) * (W/nf + 0.29)' ps='2*int((nf+2)/2) * (W/nf + 0.29)'
+ nrd='0.29 / W' nrs='0.29 / W' sa=0 sb=0 sd=0 mult=1 m=1
XM182 net21 net20 net20 GND sky130_fd_pr__nfet_01v8 L={L} W={W/2} nf=1 ad='int((nf+1)/2) * W/nf * 0.29'
+ as='int((nf+2)/2) * W/nf * 0.29' pd='2*int((nf+1)/2) * (W/nf + 0.29)' ps='2*int((nf+2)/2) * (W/nf + 0.29)'
+ nrd='0.29 / W' nrs='0.29 / W' sa=0 sb=0 sd=0 mult=1 m=1
XM183 net20 net20 net21 GND sky130_fd_pr__nfet_01v8 L={L} W={W/2} nf=1 ad='int((nf+1)/2) * W/nf * 0.29'
+ as='int((nf+2)/2) * W/nf * 0.29' pd='2*int((nf+1)/2) * (W/nf + 0.29)' ps='2*int((nf+2)/2) * (W/nf + 0.29)'
+ nrd='0.29 / W' nrs='0.29 / W' sa=0 sb=0 sd=0 mult=1 m=1
XM184 VDD VDD net28 VDD sky130_fd_pr__pfet_01v8 L={L} W={W/2} nf=1 ad='int((nf+1)/2) * W/nf * 0.29' as='int((nf+2)/2) * W/nf * 0.29'
+ pd='2*int((nf+1)/2) * (W/nf + 0.29)' ps='2*int((nf+2)/2) * (W/nf + 0.29)' nrd='0.29 / W' nrs='0.29 / W'
+ sa=0 sb=0 sd=0 mult=1 m=1
XM185 net26 VDD VDD VDD sky130_fd_pr__pfet_01v8 L={L} W={W/2} nf=1 ad='int((nf+1)/2) * W/nf * 0.29' as='int((nf+2)/2) * W/nf * 0.29'
+ pd='2*int((nf+1)/2) * (W/nf + 0.29)' ps='2*int((nf+2)/2) * (W/nf + 0.29)' nrd='0.29 / W' nrs='0.29 / W'
+ sa=0 sb=0 sd=0 mult=1 m=1
Vout net29 GND 0
.save i(vout)
XM21 net28 net22 net35 VDD sky130_fd_pr__pfet_01v8 L={L} W={W/2} nf=1 ad='int((nf+1)/2) * W/nf * 0.29'
+ as='int((nf+2)/2) * W/nf * 0.29' pd='2*int((nf+1)/2) * (W/nf + 0.29)' ps='2*int((nf+2)/2) * (W/nf + 0.29)'
+ nrd='0.29 / W' nrs='0.29 / W' sa=0 sb=0 sd=0 mult=1 m=1
XM22 net35 net22 net34 VDD sky130_fd_pr__pfet_01v8 L={L} W={W/2} nf=1 ad='int((nf+1)/2) * W/nf * 0.29'
+ as='int((nf+2)/2) * W/nf * 0.29' pd='2*int((nf+1)/2) * (W/nf + 0.29)' ps='2*int((nf+2)/2) * (W/nf + 0.29)'
+ nrd='0.29 / W' nrs='0.29 / W' sa=0 sb=0 sd=0 mult=1 m=1
XM23 net34 net22 net33 VDD sky130_fd_pr__pfet_01v8 L={L} W={W/2} nf=1 ad='int((nf+1)/2) * W/nf * 0.29'
+ as='int((nf+2)/2) * W/nf * 0.29' pd='2*int((nf+1)/2) * (W/nf + 0.29)' ps='2*int((nf+2)/2) * (W/nf + 0.29)'
+ nrd='0.29 / W' nrs='0.29 / W' sa=0 sb=0 sd=0 mult=1 m=1
XM24 net33 net22 net22 VDD sky130_fd_pr__pfet_01v8 L={L} W={W/2} nf=1 ad='int((nf+1)/2) * W/nf * 0.29'
+ as='int((nf+2)/2) * W/nf * 0.29' pd='2*int((nf+1)/2) * (W/nf + 0.29)' ps='2*int((nf+2)/2) * (W/nf + 0.29)'
+ nrd='0.29 / W' nrs='0.29 / W' sa=0 sb=0 sd=0 mult=1 m=1
XM25 net22 net22 net32 VDD sky130_fd_pr__pfet_01v8 L={L} W={W/2} nf=1 ad='int((nf+1)/2) * W/nf * 0.29'
+ as='int((nf+2)/2) * W/nf * 0.29' pd='2*int((nf+1)/2) * (W/nf + 0.29)' ps='2*int((nf+2)/2) * (W/nf + 0.29)'
+ nrd='0.29 / W' nrs='0.29 / W' sa=0 sb=0 sd=0 mult=1 m=1
XM26 net32 net22 net31 VDD sky130_fd_pr__pfet_01v8 L={L} W={W/2} nf=1 ad='int((nf+1)/2) * W/nf * 0.29'
+ as='int((nf+2)/2) * W/nf * 0.29' pd='2*int((nf+1)/2) * (W/nf + 0.29)' ps='2*int((nf+2)/2) * (W/nf + 0.29)'
+ nrd='0.29 / W' nrs='0.29 / W' sa=0 sb=0 sd=0 mult=1 m=1
XM27 net31 net22 net30 VDD sky130_fd_pr__pfet_01v8 L={L} W={W/2} nf=1 ad='int((nf+1)/2) * W/nf * 0.29'
+ as='int((nf+2)/2) * W/nf * 0.29' pd='2*int((nf+1)/2) * (W/nf + 0.29)' ps='2*int((nf+2)/2) * (W/nf + 0.29)'
+ nrd='0.29 / W' nrs='0.29 / W' sa=0 sb=0 sd=0 mult=1 m=1
XM28 net30 net22 net28 VDD sky130_fd_pr__pfet_01v8 L={L} W={W/2} nf=1 ad='int((nf+1)/2) * W/nf * 0.29'
+ as='int((nf+2)/2) * W/nf * 0.29' pd='2*int((nf+1)/2) * (W/nf + 0.29)' ps='2*int((nf+2)/2) * (W/nf + 0.29)'
+ nrd='0.29 / W' nrs='0.29 / W' sa=0 sb=0 sd=0 mult=1 m=1
XM30 net26 net25 net41 VDD sky130_fd_pr__pfet_01v8 L={L} W={W/2} nf=1 ad='int((nf+1)/2) * W/nf * 0.29'
+ as='int((nf+2)/2) * W/nf * 0.29' pd='2*int((nf+1)/2) * (W/nf + 0.29)' ps='2*int((nf+2)/2) * (W/nf + 0.29)'
+ nrd='0.29 / W' nrs='0.29 / W' sa=0 sb=0 sd=0 mult=1 m=1
XM31 net41 net25 net40 VDD sky130_fd_pr__pfet_01v8 L={L} W={W/2} nf=1 ad='int((nf+1)/2) * W/nf * 0.29'
+ as='int((nf+2)/2) * W/nf * 0.29' pd='2*int((nf+1)/2) * (W/nf + 0.29)' ps='2*int((nf+2)/2) * (W/nf + 0.29)'
+ nrd='0.29 / W' nrs='0.29 / W' sa=0 sb=0 sd=0 mult=1 m=1
XM32 net40 net25 net39 VDD sky130_fd_pr__pfet_01v8 L={L} W={W/2} nf=1 ad='int((nf+1)/2) * W/nf * 0.29'
+ as='int((nf+2)/2) * W/nf * 0.29' pd='2*int((nf+1)/2) * (W/nf + 0.29)' ps='2*int((nf+2)/2) * (W/nf + 0.29)'
+ nrd='0.29 / W' nrs='0.29 / W' sa=0 sb=0 sd=0 mult=1 m=1
XM33 net39 net25 net25 VDD sky130_fd_pr__pfet_01v8 L={L} W={W/2} nf=1 ad='int((nf+1)/2) * W/nf * 0.29'
+ as='int((nf+2)/2) * W/nf * 0.29' pd='2*int((nf+1)/2) * (W/nf + 0.29)' ps='2*int((nf+2)/2) * (W/nf + 0.29)'
+ nrd='0.29 / W' nrs='0.29 / W' sa=0 sb=0 sd=0 mult=1 m=1
XM34 net25 net25 net38 VDD sky130_fd_pr__pfet_01v8 L={L} W={W/2} nf=1 ad='int((nf+1)/2) * W/nf * 0.29'
+ as='int((nf+2)/2) * W/nf * 0.29' pd='2*int((nf+1)/2) * (W/nf + 0.29)' ps='2*int((nf+2)/2) * (W/nf + 0.29)'
+ nrd='0.29 / W' nrs='0.29 / W' sa=0 sb=0 sd=0 mult=1 m=1
XM35 net38 net25 net37 VDD sky130_fd_pr__pfet_01v8 L={L} W={W/2} nf=1 ad='int((nf+1)/2) * W/nf * 0.29'
+ as='int((nf+2)/2) * W/nf * 0.29' pd='2*int((nf+1)/2) * (W/nf + 0.29)' ps='2*int((nf+2)/2) * (W/nf + 0.29)'
+ nrd='0.29 / W' nrs='0.29 / W' sa=0 sb=0 sd=0 mult=1 m=1
XM36 net37 net25 net36 VDD sky130_fd_pr__pfet_01v8 L={L} W={W/2} nf=1 ad='int((nf+1)/2) * W/nf * 0.29'
+ as='int((nf+2)/2) * W/nf * 0.29' pd='2*int((nf+1)/2) * (W/nf + 0.29)' ps='2*int((nf+2)/2) * (W/nf + 0.29)'
+ nrd='0.29 / W' nrs='0.29 / W' sa=0 sb=0 sd=0 mult=1 m=1
XM37 net36 net25 net26 VDD sky130_fd_pr__pfet_01v8 L={L} W={W/2} nf=1 ad='int((nf+1)/2) * W/nf * 0.29'
+ as='int((nf+2)/2) * W/nf * 0.29' pd='2*int((nf+1)/2) * (W/nf + 0.29)' ps='2*int((nf+2)/2) * (W/nf + 0.29)'
+ nrd='0.29 / W' nrs='0.29 / W' sa=0 sb=0 sd=0 mult=1 m=1
**** begin user architecture code

.param W=3
.param L=0.5
.control
set wr_vecnames
set wr_singlescale
let code = 0
  while code < 128
    if code eq 0
      let b0 = 0
    else
      let b0 = code % 2 * 1.8
    end
    if floor(code / 2) eq 0
      let b1 = 0
    else
      let b1 = floor(code / 2) % 2 * 1.8
    end
    if floor(code / 4) eq 0
      let b2 = 0
    else
      let b2 = floor(code / 4) % 2 * 1.8
    end
    if floor(code / 8) eq 0
      let b3 = 0
    else
      let b3 = floor(code / 8) % 2 * 1.8
    end
    if floor(code / 16) eq 0
      let b4 = 0
    else
      let b4 = floor(code / 16) % 2 * 1.8
    end
    if floor(code / 32) eq 0
      let b5 = 0
    else
      let b5 = floor(code / 32) % 2 * 1.8
    end
    if floor(code / 64) eq 0
      let b6 = 0
    else
      let b6 = floor(code / 64) % 2 * 1.8
    end
    alter v0 $&b0
    alter v1 $&b1
    alter v2 $&b2
    alter v3 $&b3
    alter v4 $&b4
    alter v5 $&b5
    alter v6 $&b6
    save all
    op
    wrdata ~/Documents/current-output-dac-vlsi/simulations/dac_sim.txt v(Vbn) i(Vout) i(Vout1) v(b6)
+ v(b5) v(b4) v(b3) v(b2) v(b1) v(b0) v(b0out) v(b1out) v(b6out)
    if code eq 0
      set appendwrite
      set wr_vecnames = FALSE
    end
    let code = code + 1
  end
.endc


.option wnflag=1
.param MC_SWITCH=0.0
.lib ~/skywater/skywater-pdk/libraries/sky130_fd_pr_ngspice/latest/models/sky130.lib.spice tt

**** end user architecture code
**.ends

* expanding   symbol:  /home/madvlsi/Documents/current-output-dac-vlsi/schematics/mux.sym # of
*+ pins=4
** sym_path: /home/madvlsi/Documents/current-output-dac-vlsi/schematics/mux.sym
** sch_path: /home/madvlsi/Documents/current-output-dac-vlsi/schematics/mux.sch
.subckt mux A B Y S
*.ipin S
*.ipin A
*.opin Y
*.ipin B
XM1 net1 S GND GND sky130_fd_pr__nfet_01v8 L=0.15 W=1 nf=1 ad='int((nf+1)/2) * W/nf * 0.29' as='int((nf+2)/2) * W/nf * 0.29'
+ pd='2*int((nf+1)/2) * (W/nf + 0.29)' ps='2*int((nf+2)/2) * (W/nf + 0.29)' nrd='0.29 / W' nrs='0.29 / W'
+ sa=0 sb=0 sd=0 mult=1 m=1
XM2 net1 S VDD VDD sky130_fd_pr__pfet_01v8 L=0.15 W=1 nf=1 ad='int((nf+1)/2) * W/nf * 0.29' as='int((nf+2)/2) * W/nf * 0.29'
+ pd='2*int((nf+1)/2) * (W/nf + 0.29)' ps='2*int((nf+2)/2) * (W/nf + 0.29)' nrd='0.29 / W' nrs='0.29 / W'
+ sa=0 sb=0 sd=0 mult=1 m=1
XM3 Y S B GND sky130_fd_pr__nfet_01v8 L=0.15 W=1 nf=1 ad='int((nf+1)/2) * W/nf * 0.29' as='int((nf+2)/2) * W/nf * 0.29'
+ pd='2*int((nf+1)/2) * (W/nf + 0.29)' ps='2*int((nf+2)/2) * (W/nf + 0.29)' nrd='0.29 / W' nrs='0.29 / W'
+ sa=0 sb=0 sd=0 mult=1 m=1
XM4 A net1 Y GND sky130_fd_pr__nfet_01v8 L=0.15 W=1 nf=1 ad='int((nf+1)/2) * W/nf * 0.29' as='int((nf+2)/2) * W/nf * 0.29'
+ pd='2*int((nf+1)/2) * (W/nf + 0.29)' ps='2*int((nf+2)/2) * (W/nf + 0.29)' nrd='0.29 / W' nrs='0.29 / W'
+ sa=0 sb=0 sd=0 mult=1 m=1
.ends

.GLOBAL GND
.GLOBAL VDD
.end
